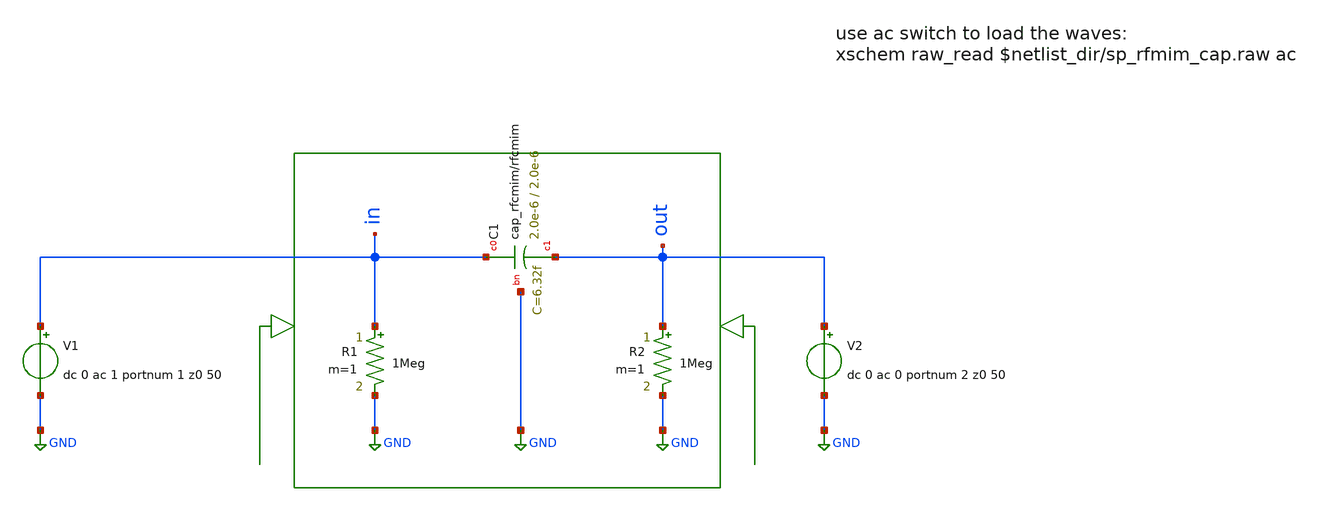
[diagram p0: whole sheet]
** sch_path: ihp-sg13g2/xschem_libs/sg13g2_tests_ase/sp_rfmim_cap/schematic/sp_rfmim_cap.sch
* Copyright 2021 Stefan Frederik Schippers
* Licensed under the Apache License, Version 2.0 (the "License");
* you may not use this file except in compliance with the License.
* You may obtain a copy of the License at
* https://www.apache.org/licenses/LICENSE-2.0
* Unless required by applicable law or agreed to in writing, software
* distributed under the License is distributed on an "AS IS" BASIS,
* WITHOUT WARRANTIES OR CONDITIONS OF ANY KIND, either express or implied.
* See the License for the specific language governing permissions and
* limitations under the License.
* Copyright 2023 IHP PDK Authors
**.subckt sp_rfmim_cap
R1 in GND 1Meg m=1
V1 in GND dc 0 ac 1 portnum 1 z0 50
R2 out GND 1Meg m=1
V2 out GND dc 0 ac 0 portnum 2 z0 50
XC1 in out GND cap_rfcmim w=2.0e-6 l=2.0e-6 wfeed=5.0e-6 m=1 mm_ok=1
**.ends
.GLOBAL GND
.end
